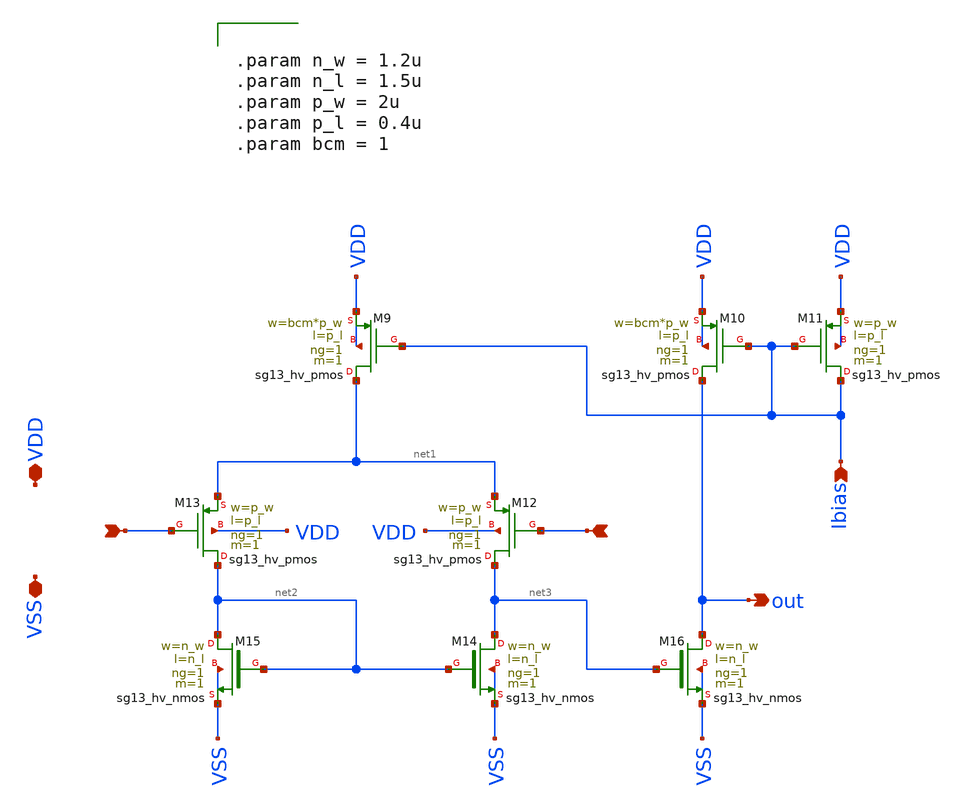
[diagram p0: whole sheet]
** sch_path: macros/heichips26_vcr/macros/switched_capacitor/schematic/xschem/comp_pmos.sch
**.subckt comp_pmos VDD VSS Ibias out + -
*.iopin VDD
*.iopin VSS
*.ipin Ibias
*.opin out
*.ipin +
*.ipin -
XM9 net1 Ibias VDD VDD sg13_hv_pmos w=bcm*p_w l=p_l ng=1 m=1 mm_ok=1
XM10 out Ibias VDD VDD sg13_hv_pmos w=bcm*p_w l=p_l ng=1 m=1 mm_ok=1
XM11 Ibias Ibias VDD VDD sg13_hv_pmos w=p_w l=p_l ng=1 m=1 mm_ok=1
XM12 net3 + net1 VDD sg13_hv_pmos w=p_w l=p_l ng=1 m=1 mm_ok=1
XM13 net2 - net1 VDD sg13_hv_pmos w=p_w l=p_l ng=1 m=1 mm_ok=1
XM14 net3 net2 VSS VSS sg13_hv_nmos w=n_w l=n_l ng=1 m=1 mm_ok=1
XM15 net2 net2 VSS VSS sg13_hv_nmos w=n_w l=n_l ng=1 m=1 mm_ok=1
XM16 out net3 VSS VSS sg13_hv_nmos w=n_w l=n_l ng=1 m=1 mm_ok=1
**** begin user architecture code


.param n_w = 1.2u
.param n_l = 1.5u
.param p_w = 2u
.param p_l = 0.4u
.param bcm = 1


**** end user architecture code
**.ends
.end
